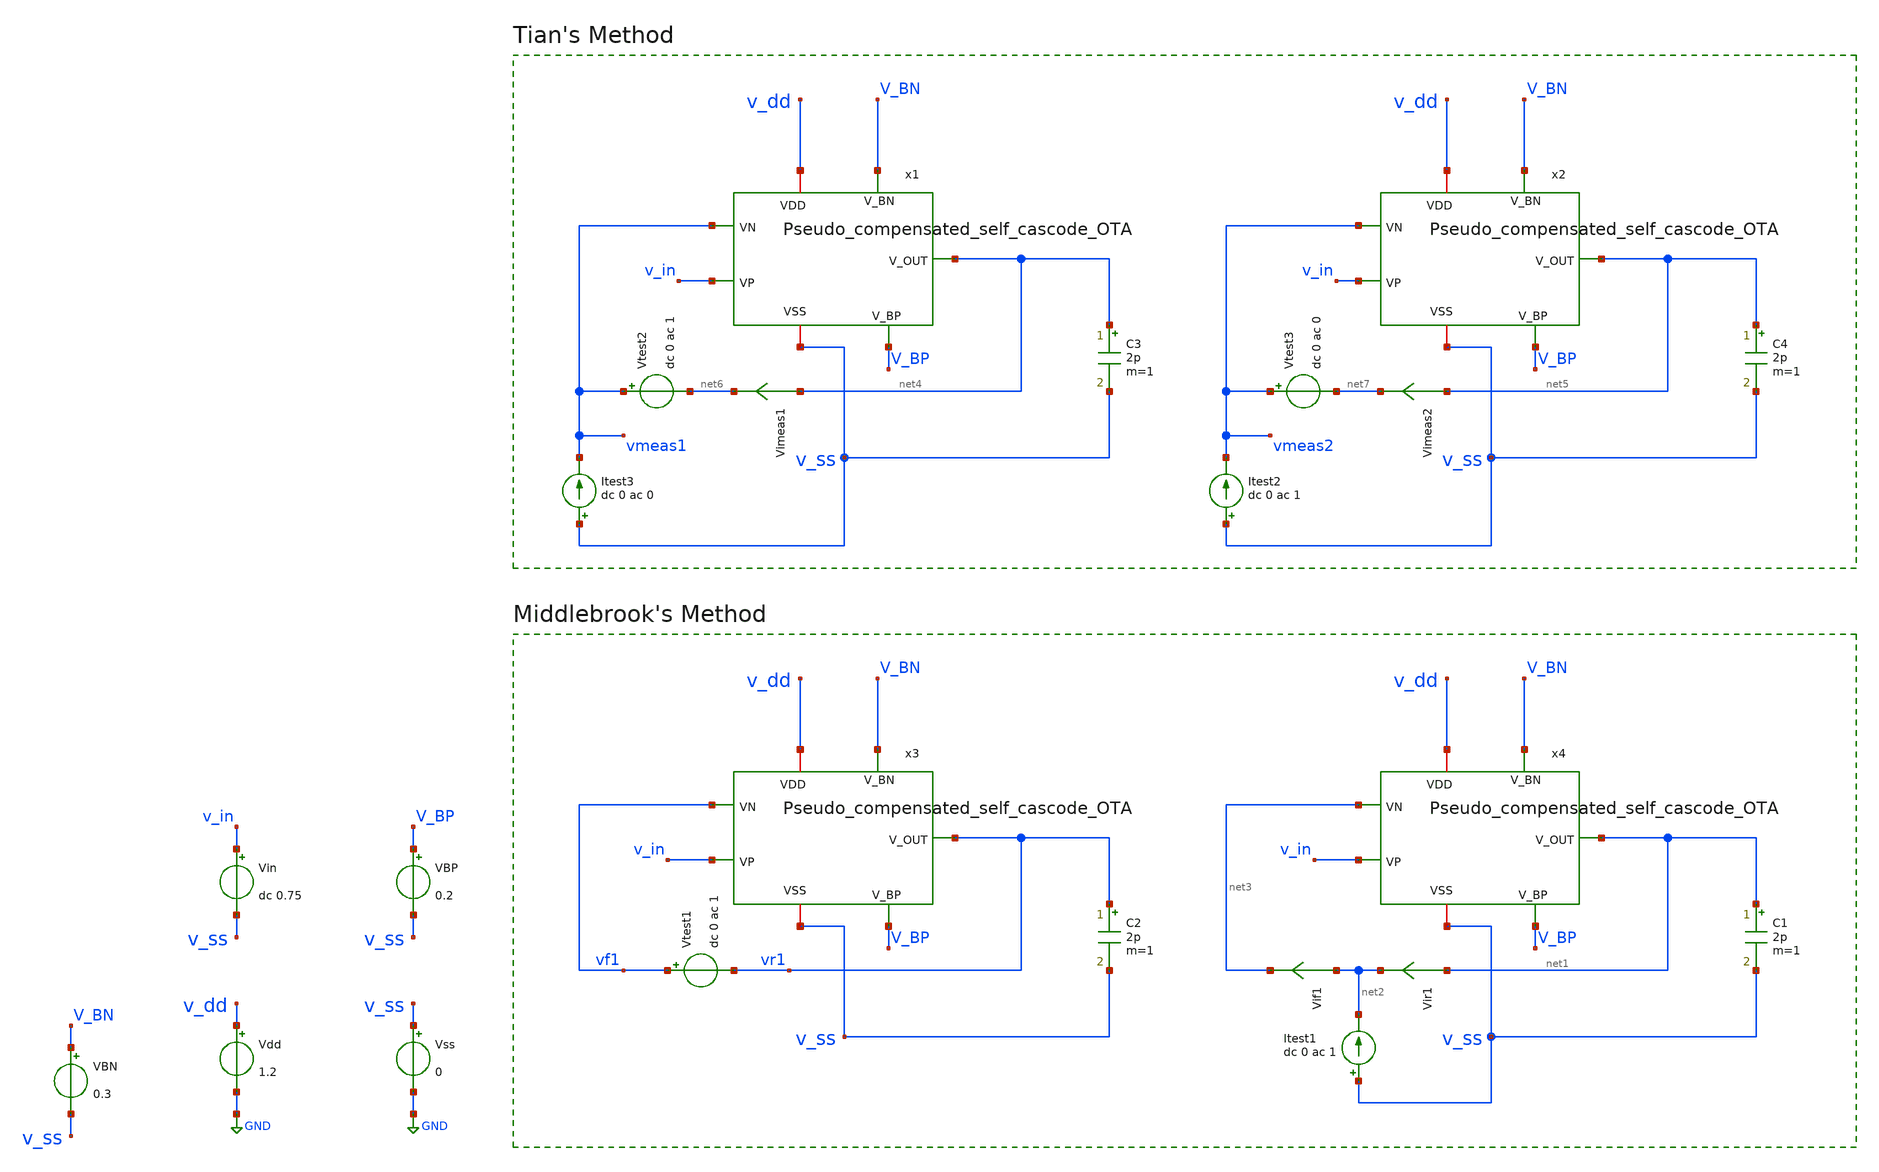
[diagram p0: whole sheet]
** sch_path: xschem/OTA_tb_loopgain.sch
**.subckt OTA_tb_loopgain
Vdd v_dd GND 1.2
Vss v_ss GND 0
Vin v_in v_ss dc 0.75
VBP V_BP v_ss 0.2
C2 vr1 v_ss 2p m=1
Vtest1 vf1 vr1 dc 0 ac 1
C1 net1 v_ss 2p m=1
Vir1 net1 net2 0
.save i(vir1)
Vif1 net2 net3 0
.save i(vif1)
Itest1 v_ss net2 dc 0 ac 1
C3 net4 v_ss 2p m=1
C4 net5 v_ss 2p m=1
Itest3 v_ss vmeas1 dc 0 ac 0
Vtest2 vmeas1 net6 dc 0 ac 1
Vimeas1 net4 net6 0
.save i(vimeas1)
Itest2 v_ss vmeas2 dc 0 ac 1
Vtest3 vmeas2 net7 dc 0 ac 0
Vimeas2 net5 net7 0
.save i(vimeas2)
x1 vmeas1 v_in V_BN V_BP net4 v_dd v_ss Pseudo_compensated_self_cascode_OTA
VBN V_BN v_ss 0.3
x2 vmeas2 v_in V_BN V_BP net5 v_dd v_ss Pseudo_compensated_self_cascode_OTA
x3 vf1 v_in V_BN V_BP vr1 v_dd v_ss Pseudo_compensated_self_cascode_OTA
x4 net3 v_in V_BN V_BP net1 v_dd v_ss Pseudo_compensated_self_cascode_OTA
**** begin user architecture code
 .lib cornerMOSlv.lib mos_tt



.param temp=27
.options savecurrents reltol=1e-3 abstol=1e-12 gmin=1e-15
.control
save all

* Operating Point Analysis
op
remzerovec
write ota-5t_tb-loopgain.raw
set appendwrite

* AC Analysis
ac dec 101 1 100G
remzerovec
write ota-5t_tb-loopgain.raw
set appendwrite

* Middlebrook's Method
let tv=-v(vr1)/v(vf1)
let ti=-i(vir1)/i(vif1)
let tmb=(tv*ti - 1)/(tv + ti + 2)

plot db(tmb) ylabel 'Magnitude - Middlebrook'
plot 180/pi*cphase(tmb) ylabel 'Phase - Middlebrook'

* Tian's Method
* vtest=0, itest=1:
let A=i(Vimeas2)
let C=v(vmeas2)

* vtest=1, itest=0:
let B=i(Vimeas1)
let D=v(vmeas1)
let ttian=(A*D-B*C-A)/(2*(B*C-A*D)+A-D+1)

plot db(ttian) ylabel 'Magnitude - Tian'
plot 180/pi*cphase(ttian) ylabel 'Phase - Tian'

* Middlebrook vs. Tian
plot db(tmb) db(ttian) ylabel 'Magnitude'
plot 180/pi*cphase(tmb) 180/pi*cphase(ttian) ylabel 'Phase'

write ota-5t_tb-loopgain.raw

*quit
.endc


**** end user architecture code
**.ends

* expanding   symbol:  Pseudo_compensated_self_cascode_OTA.sym # of pins=7
** sym_path: xschem/Pseudo_compensated_self_cascode_OTA.sym
** sch_path: xschem/Pseudo_compensated_self_cascode_OTA.sch
.subckt Pseudo_compensated_self_cascode_OTA VN VP V_BN V_BP V_OUT VDD VSS
*.ipin VN
*.ipin VP
*.ipin V_BN
*.ipin V_BP
*.opin V_OUT
*.iopin VDD
*.iopin VSS
XM11 net1 VN net2 VSS sg13_lv_nmos w=70u l=0.8u ng=7 m=1 mm_ok=1
XM12 V_GS VN net1 V_BP sg13_lv_nmos w=38.5u l=0.3u ng=4 m=1 mm_ok=1
XM21 net4 VP net2 VSS sg13_lv_nmos w=70u l=0.8u ng=7 m=1 mm_ok=1
XM22 VB32 VP net4 V_BP sg13_lv_nmos w=38.5u l=0.3u ng=4 m=1 mm_ok=1
XM52 net2 V_BN net3 V_BN sg13_lv_nmos w=40u l=0.5u ng=4 m=1 mm_ok=1
XM51 net3 V_BN VSS VSS sg13_lv_nmos w=40u l=2.5u ng=4 m=1 mm_ok=1
XM32 V_GS V_GS VS32 VB32 sg13_lv_pmos w=48.5u l=1.24u ng=5 m=1 mm_ok=1
XM31 VS32 V_GS VDD VDD sg13_lv_pmos w=48.5u l=0.87u ng=5 m=1 mm_ok=1
XM42 VB32 V_GS VS42 V_GS sg13_lv_pmos w=48.5u l=1.24u ng=5 m=1 mm_ok=1
XM41 VS42 V_GS VDD VDD sg13_lv_pmos w=48.5u l=0.87u ng=5 m=1 mm_ok=1
XM61 net5 VB32 VDD VDD sg13_lv_pmos w=60u l=0.13u ng=6 m=1 mm_ok=1
XM62 V_OUT VB32 net5 V_BP sg13_lv_pmos w=60u l=0.13u ng=6 m=1 mm_ok=1
XM72 V_OUT V_BN net6 V_BN sg13_lv_nmos w=40u l=0.5u ng=10 m=1 mm_ok=1
XM71 net6 V_BN VSS VSS sg13_lv_nmos w=40u l=2.5u ng=4 m=1 mm_ok=1
XC3 VS42 V_OUT cap_cmim w=5.0e-6 l=5.0e-6 m=38 mm_ok=1
XC1 net4 V_OUT cap_cmim w=5.0e-6 l=5.0e-6 m=38 mm_ok=1
.ends

.GLOBAL GND
.end
